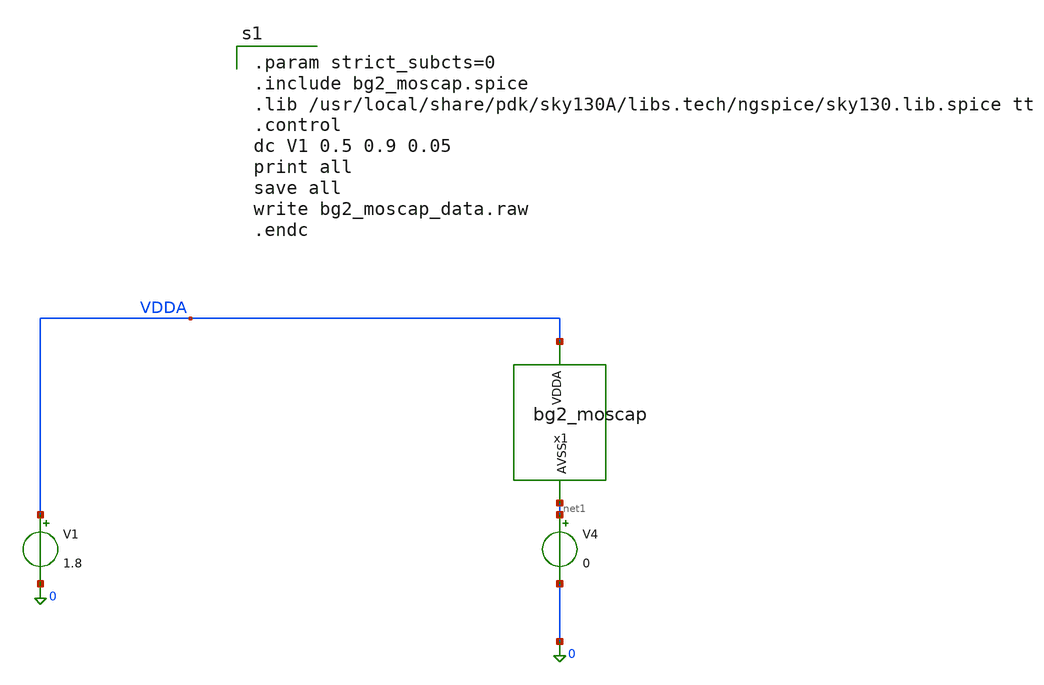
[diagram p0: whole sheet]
** sch_path: gds/bg2_moscap_tb.sch
**.subckt bg2_moscap_tb
V1 VDDA 0 1.8
V4 net1 0 0
x1 VDDA net1 bg2_moscap
**** begin user architecture code

.param strict_subcts=0
.include bg2_moscap.spice
.lib /usr/local/share/pdk/sky130A/libs.tech/ngspice/sky130.lib.spice tt
.control
dc V1 0.5 0.9 0.05
print all
save all
write bg2_moscap_data.raw
.endc

**** end user architecture code
**.ends
.end
